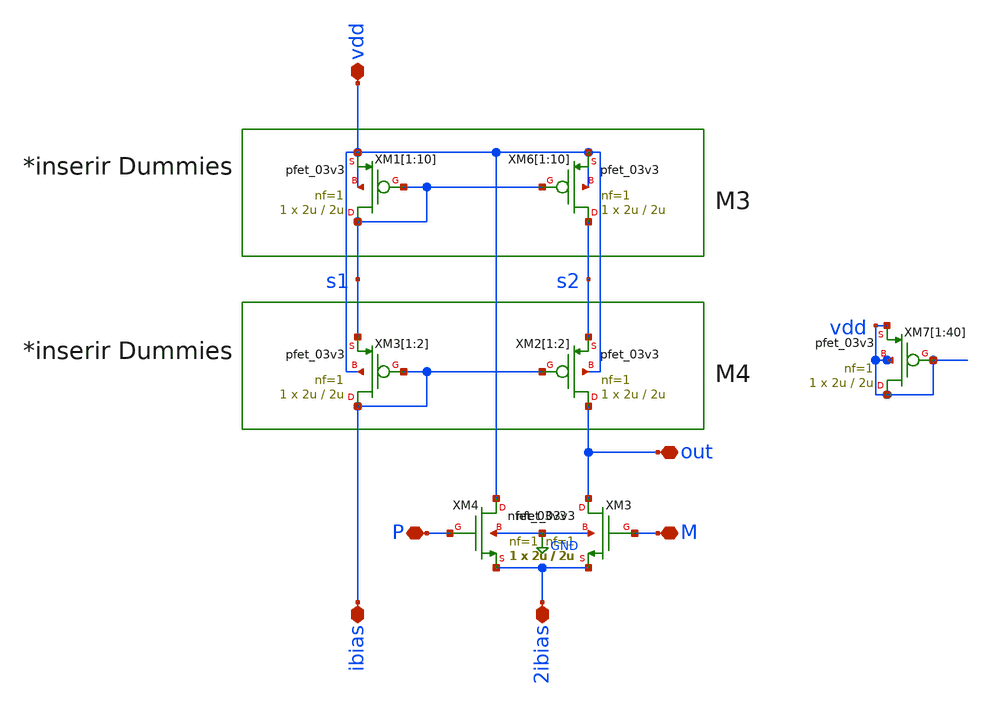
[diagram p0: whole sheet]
** sch_path: Clock_Reference/symbols_clock/VCIS.sch
**.subckt VCIS 2ibias ibias P M out vdd
*.iopin 2ibias
*.iopin ibias
*.iopin P
*.iopin M
*.iopin out
*.iopin vdd
XM2[1] out ibias s2 vdd pfet_03v3 L=2u W=2u nf=1 ad='int((nf+1)/2) * W/nf * 0.18u' as='int((nf+2)/2) * W/nf * 0.18u'
+ pd='2*int((nf+1)/2) * (W/nf + 0.18u)' ps='2*int((nf+2)/2) * (W/nf + 0.18u)' nrd='0.18u / W' nrs='0.18u / W'
+ sa=0 sb=0 sd=0 m=1
XM2[2] out ibias s2 vdd pfet_03v3 L=2u W=2u nf=1 ad='int((nf+1)/2) * W/nf * 0.18u' as='int((nf+2)/2) * W/nf * 0.18u'
+ pd='2*int((nf+1)/2) * (W/nf + 0.18u)' ps='2*int((nf+2)/2) * (W/nf + 0.18u)' nrd='0.18u / W' nrs='0.18u / W'
+ sa=0 sb=0 sd=0 m=1
XM3[1] ibias ibias s1 vdd pfet_03v3 L=2u W=2u nf=1 ad='int((nf+1)/2) * W/nf * 0.18u' as='int((nf+2)/2) * W/nf * 0.18u'
+ pd='2*int((nf+1)/2) * (W/nf + 0.18u)' ps='2*int((nf+2)/2) * (W/nf + 0.18u)' nrd='0.18u / W' nrs='0.18u / W'
+ sa=0 sb=0 sd=0 m=1
XM3[2] ibias ibias s1 vdd pfet_03v3 L=2u W=2u nf=1 ad='int((nf+1)/2) * W/nf * 0.18u' as='int((nf+2)/2) * W/nf * 0.18u'
+ pd='2*int((nf+1)/2) * (W/nf + 0.18u)' ps='2*int((nf+2)/2) * (W/nf + 0.18u)' nrd='0.18u / W' nrs='0.18u / W'
+ sa=0 sb=0 sd=0 m=1
XM3 out M 2ibias GND nfet_03v3 L=2u W=2u nf=1 ad='int((nf+1)/2) * W/nf * 0.18u' as='int((nf+2)/2) * W/nf * 0.18u'
+ pd='2*int((nf+1)/2) * (W/nf + 0.18u)' ps='2*int((nf+2)/2) * (W/nf + 0.18u)' nrd='0.18u / W' nrs='0.18u / W'
+ sa=0 sb=0 sd=0 m=1
XM4 vdd P 2ibias GND nfet_03v3 L=2u W=2u nf=1 ad='int((nf+1)/2) * W/nf * 0.18u' as='int((nf+2)/2) * W/nf * 0.18u'
+ pd='2*int((nf+1)/2) * (W/nf + 0.18u)' ps='2*int((nf+2)/2) * (W/nf + 0.18u)' nrd='0.18u / W' nrs='0.18u / W'
+ sa=0 sb=0 sd=0 m=1
XM6[1] s2 s1 vdd vdd pfet_03v3 L=2u W=2u nf=1 ad='int((nf+1)/2) * W/nf * 0.18u' as='int((nf+2)/2) * W/nf * 0.18u'
+ pd='2*int((nf+1)/2) * (W/nf + 0.18u)' ps='2*int((nf+2)/2) * (W/nf + 0.18u)' nrd='0.18u / W' nrs='0.18u / W'
+ sa=0 sb=0 sd=0 m=1
XM6[2] s2 s1 vdd vdd pfet_03v3 L=2u W=2u nf=1 ad='int((nf+1)/2) * W/nf * 0.18u' as='int((nf+2)/2) * W/nf * 0.18u'
+ pd='2*int((nf+1)/2) * (W/nf + 0.18u)' ps='2*int((nf+2)/2) * (W/nf + 0.18u)' nrd='0.18u / W' nrs='0.18u / W'
+ sa=0 sb=0 sd=0 m=1
XM6[3] s2 s1 vdd vdd pfet_03v3 L=2u W=2u nf=1 ad='int((nf+1)/2) * W/nf * 0.18u' as='int((nf+2)/2) * W/nf * 0.18u'
+ pd='2*int((nf+1)/2) * (W/nf + 0.18u)' ps='2*int((nf+2)/2) * (W/nf + 0.18u)' nrd='0.18u / W' nrs='0.18u / W'
+ sa=0 sb=0 sd=0 m=1
XM6[4] s2 s1 vdd vdd pfet_03v3 L=2u W=2u nf=1 ad='int((nf+1)/2) * W/nf * 0.18u' as='int((nf+2)/2) * W/nf * 0.18u'
+ pd='2*int((nf+1)/2) * (W/nf + 0.18u)' ps='2*int((nf+2)/2) * (W/nf + 0.18u)' nrd='0.18u / W' nrs='0.18u / W'
+ sa=0 sb=0 sd=0 m=1
XM6[5] s2 s1 vdd vdd pfet_03v3 L=2u W=2u nf=1 ad='int((nf+1)/2) * W/nf * 0.18u' as='int((nf+2)/2) * W/nf * 0.18u'
+ pd='2*int((nf+1)/2) * (W/nf + 0.18u)' ps='2*int((nf+2)/2) * (W/nf + 0.18u)' nrd='0.18u / W' nrs='0.18u / W'
+ sa=0 sb=0 sd=0 m=1
XM6[6] s2 s1 vdd vdd pfet_03v3 L=2u W=2u nf=1 ad='int((nf+1)/2) * W/nf * 0.18u' as='int((nf+2)/2) * W/nf * 0.18u'
+ pd='2*int((nf+1)/2) * (W/nf + 0.18u)' ps='2*int((nf+2)/2) * (W/nf + 0.18u)' nrd='0.18u / W' nrs='0.18u / W'
+ sa=0 sb=0 sd=0 m=1
XM6[7] s2 s1 vdd vdd pfet_03v3 L=2u W=2u nf=1 ad='int((nf+1)/2) * W/nf * 0.18u' as='int((nf+2)/2) * W/nf * 0.18u'
+ pd='2*int((nf+1)/2) * (W/nf + 0.18u)' ps='2*int((nf+2)/2) * (W/nf + 0.18u)' nrd='0.18u / W' nrs='0.18u / W'
+ sa=0 sb=0 sd=0 m=1
XM6[8] s2 s1 vdd vdd pfet_03v3 L=2u W=2u nf=1 ad='int((nf+1)/2) * W/nf * 0.18u' as='int((nf+2)/2) * W/nf * 0.18u'
+ pd='2*int((nf+1)/2) * (W/nf + 0.18u)' ps='2*int((nf+2)/2) * (W/nf + 0.18u)' nrd='0.18u / W' nrs='0.18u / W'
+ sa=0 sb=0 sd=0 m=1
XM6[9] s2 s1 vdd vdd pfet_03v3 L=2u W=2u nf=1 ad='int((nf+1)/2) * W/nf * 0.18u' as='int((nf+2)/2) * W/nf * 0.18u'
+ pd='2*int((nf+1)/2) * (W/nf + 0.18u)' ps='2*int((nf+2)/2) * (W/nf + 0.18u)' nrd='0.18u / W' nrs='0.18u / W'
+ sa=0 sb=0 sd=0 m=1
XM6[10] s2 s1 vdd vdd pfet_03v3 L=2u W=2u nf=1 ad='int((nf+1)/2) * W/nf * 0.18u' as='int((nf+2)/2) * W/nf * 0.18u'
+ pd='2*int((nf+1)/2) * (W/nf + 0.18u)' ps='2*int((nf+2)/2) * (W/nf + 0.18u)' nrd='0.18u / W' nrs='0.18u / W'
+ sa=0 sb=0 sd=0 m=1
XM1[1] s1 s1 vdd vdd pfet_03v3 L=2u W=2u nf=1 ad='int((nf+1)/2) * W/nf * 0.18u' as='int((nf+2)/2) * W/nf * 0.18u'
+ pd='2*int((nf+1)/2) * (W/nf + 0.18u)' ps='2*int((nf+2)/2) * (W/nf + 0.18u)' nrd='0.18u / W' nrs='0.18u / W'
+ sa=0 sb=0 sd=0 m=1
XM1[2] s1 s1 vdd vdd pfet_03v3 L=2u W=2u nf=1 ad='int((nf+1)/2) * W/nf * 0.18u' as='int((nf+2)/2) * W/nf * 0.18u'
+ pd='2*int((nf+1)/2) * (W/nf + 0.18u)' ps='2*int((nf+2)/2) * (W/nf + 0.18u)' nrd='0.18u / W' nrs='0.18u / W'
+ sa=0 sb=0 sd=0 m=1
XM1[3] s1 s1 vdd vdd pfet_03v3 L=2u W=2u nf=1 ad='int((nf+1)/2) * W/nf * 0.18u' as='int((nf+2)/2) * W/nf * 0.18u'
+ pd='2*int((nf+1)/2) * (W/nf + 0.18u)' ps='2*int((nf+2)/2) * (W/nf + 0.18u)' nrd='0.18u / W' nrs='0.18u / W'
+ sa=0 sb=0 sd=0 m=1
XM1[4] s1 s1 vdd vdd pfet_03v3 L=2u W=2u nf=1 ad='int((nf+1)/2) * W/nf * 0.18u' as='int((nf+2)/2) * W/nf * 0.18u'
+ pd='2*int((nf+1)/2) * (W/nf + 0.18u)' ps='2*int((nf+2)/2) * (W/nf + 0.18u)' nrd='0.18u / W' nrs='0.18u / W'
+ sa=0 sb=0 sd=0 m=1
XM1[5] s1 s1 vdd vdd pfet_03v3 L=2u W=2u nf=1 ad='int((nf+1)/2) * W/nf * 0.18u' as='int((nf+2)/2) * W/nf * 0.18u'
+ pd='2*int((nf+1)/2) * (W/nf + 0.18u)' ps='2*int((nf+2)/2) * (W/nf + 0.18u)' nrd='0.18u / W' nrs='0.18u / W'
+ sa=0 sb=0 sd=0 m=1
XM1[6] s1 s1 vdd vdd pfet_03v3 L=2u W=2u nf=1 ad='int((nf+1)/2) * W/nf * 0.18u' as='int((nf+2)/2) * W/nf * 0.18u'
+ pd='2*int((nf+1)/2) * (W/nf + 0.18u)' ps='2*int((nf+2)/2) * (W/nf + 0.18u)' nrd='0.18u / W' nrs='0.18u / W'
+ sa=0 sb=0 sd=0 m=1
XM1[7] s1 s1 vdd vdd pfet_03v3 L=2u W=2u nf=1 ad='int((nf+1)/2) * W/nf * 0.18u' as='int((nf+2)/2) * W/nf * 0.18u'
+ pd='2*int((nf+1)/2) * (W/nf + 0.18u)' ps='2*int((nf+2)/2) * (W/nf + 0.18u)' nrd='0.18u / W' nrs='0.18u / W'
+ sa=0 sb=0 sd=0 m=1
XM1[8] s1 s1 vdd vdd pfet_03v3 L=2u W=2u nf=1 ad='int((nf+1)/2) * W/nf * 0.18u' as='int((nf+2)/2) * W/nf * 0.18u'
+ pd='2*int((nf+1)/2) * (W/nf + 0.18u)' ps='2*int((nf+2)/2) * (W/nf + 0.18u)' nrd='0.18u / W' nrs='0.18u / W'
+ sa=0 sb=0 sd=0 m=1
XM1[9] s1 s1 vdd vdd pfet_03v3 L=2u W=2u nf=1 ad='int((nf+1)/2) * W/nf * 0.18u' as='int((nf+2)/2) * W/nf * 0.18u'
+ pd='2*int((nf+1)/2) * (W/nf + 0.18u)' ps='2*int((nf+2)/2) * (W/nf + 0.18u)' nrd='0.18u / W' nrs='0.18u / W'
+ sa=0 sb=0 sd=0 m=1
XM1[10] s1 s1 vdd vdd pfet_03v3 L=2u W=2u nf=1 ad='int((nf+1)/2) * W/nf * 0.18u' as='int((nf+2)/2) * W/nf * 0.18u'
+ pd='2*int((nf+1)/2) * (W/nf + 0.18u)' ps='2*int((nf+2)/2) * (W/nf + 0.18u)' nrd='0.18u / W' nrs='0.18u / W'
+ sa=0 sb=0 sd=0 m=1
XM7[1] vdd vdd vdd vdd pfet_03v3 L=2u W=2u nf=1 ad='int((nf+1)/2) * W/nf * 0.18u' as='int((nf+2)/2) * W/nf * 0.18u'
+ pd='2*int((nf+1)/2) * (W/nf + 0.18u)' ps='2*int((nf+2)/2) * (W/nf + 0.18u)' nrd='0.18u / W' nrs='0.18u / W'
+ sa=0 sb=0 sd=0 m=1
XM7[2] vdd vdd vdd vdd pfet_03v3 L=2u W=2u nf=1 ad='int((nf+1)/2) * W/nf * 0.18u' as='int((nf+2)/2) * W/nf * 0.18u'
+ pd='2*int((nf+1)/2) * (W/nf + 0.18u)' ps='2*int((nf+2)/2) * (W/nf + 0.18u)' nrd='0.18u / W' nrs='0.18u / W'
+ sa=0 sb=0 sd=0 m=1
XM7[3] vdd vdd vdd vdd pfet_03v3 L=2u W=2u nf=1 ad='int((nf+1)/2) * W/nf * 0.18u' as='int((nf+2)/2) * W/nf * 0.18u'
+ pd='2*int((nf+1)/2) * (W/nf + 0.18u)' ps='2*int((nf+2)/2) * (W/nf + 0.18u)' nrd='0.18u / W' nrs='0.18u / W'
+ sa=0 sb=0 sd=0 m=1
XM7[4] vdd vdd vdd vdd pfet_03v3 L=2u W=2u nf=1 ad='int((nf+1)/2) * W/nf * 0.18u' as='int((nf+2)/2) * W/nf * 0.18u'
+ pd='2*int((nf+1)/2) * (W/nf + 0.18u)' ps='2*int((nf+2)/2) * (W/nf + 0.18u)' nrd='0.18u / W' nrs='0.18u / W'
+ sa=0 sb=0 sd=0 m=1
XM7[5] vdd vdd vdd vdd pfet_03v3 L=2u W=2u nf=1 ad='int((nf+1)/2) * W/nf * 0.18u' as='int((nf+2)/2) * W/nf * 0.18u'
+ pd='2*int((nf+1)/2) * (W/nf + 0.18u)' ps='2*int((nf+2)/2) * (W/nf + 0.18u)' nrd='0.18u / W' nrs='0.18u / W'
+ sa=0 sb=0 sd=0 m=1
XM7[6] vdd vdd vdd vdd pfet_03v3 L=2u W=2u nf=1 ad='int((nf+1)/2) * W/nf * 0.18u' as='int((nf+2)/2) * W/nf * 0.18u'
+ pd='2*int((nf+1)/2) * (W/nf + 0.18u)' ps='2*int((nf+2)/2) * (W/nf + 0.18u)' nrd='0.18u / W' nrs='0.18u / W'
+ sa=0 sb=0 sd=0 m=1
XM7[7] vdd vdd vdd vdd pfet_03v3 L=2u W=2u nf=1 ad='int((nf+1)/2) * W/nf * 0.18u' as='int((nf+2)/2) * W/nf * 0.18u'
+ pd='2*int((nf+1)/2) * (W/nf + 0.18u)' ps='2*int((nf+2)/2) * (W/nf + 0.18u)' nrd='0.18u / W' nrs='0.18u / W'
+ sa=0 sb=0 sd=0 m=1
XM7[8] vdd vdd vdd vdd pfet_03v3 L=2u W=2u nf=1 ad='int((nf+1)/2) * W/nf * 0.18u' as='int((nf+2)/2) * W/nf * 0.18u'
+ pd='2*int((nf+1)/2) * (W/nf + 0.18u)' ps='2*int((nf+2)/2) * (W/nf + 0.18u)' nrd='0.18u / W' nrs='0.18u / W'
+ sa=0 sb=0 sd=0 m=1
XM7[9] vdd vdd vdd vdd pfet_03v3 L=2u W=2u nf=1 ad='int((nf+1)/2) * W/nf * 0.18u' as='int((nf+2)/2) * W/nf * 0.18u'
+ pd='2*int((nf+1)/2) * (W/nf + 0.18u)' ps='2*int((nf+2)/2) * (W/nf + 0.18u)' nrd='0.18u / W' nrs='0.18u / W'
+ sa=0 sb=0 sd=0 m=1
XM7[10] vdd vdd vdd vdd pfet_03v3 L=2u W=2u nf=1 ad='int((nf+1)/2) * W/nf * 0.18u' as='int((nf+2)/2) * W/nf * 0.18u'
+ pd='2*int((nf+1)/2) * (W/nf + 0.18u)' ps='2*int((nf+2)/2) * (W/nf + 0.18u)' nrd='0.18u / W' nrs='0.18u / W'
+ sa=0 sb=0 sd=0 m=1
XM7[11] vdd vdd vdd vdd pfet_03v3 L=2u W=2u nf=1 ad='int((nf+1)/2) * W/nf * 0.18u' as='int((nf+2)/2) * W/nf * 0.18u'
+ pd='2*int((nf+1)/2) * (W/nf + 0.18u)' ps='2*int((nf+2)/2) * (W/nf + 0.18u)' nrd='0.18u / W' nrs='0.18u / W'
+ sa=0 sb=0 sd=0 m=1
XM7[12] vdd vdd vdd vdd pfet_03v3 L=2u W=2u nf=1 ad='int((nf+1)/2) * W/nf * 0.18u' as='int((nf+2)/2) * W/nf * 0.18u'
+ pd='2*int((nf+1)/2) * (W/nf + 0.18u)' ps='2*int((nf+2)/2) * (W/nf + 0.18u)' nrd='0.18u / W' nrs='0.18u / W'
+ sa=0 sb=0 sd=0 m=1
XM7[13] vdd vdd vdd vdd pfet_03v3 L=2u W=2u nf=1 ad='int((nf+1)/2) * W/nf * 0.18u' as='int((nf+2)/2) * W/nf * 0.18u'
+ pd='2*int((nf+1)/2) * (W/nf + 0.18u)' ps='2*int((nf+2)/2) * (W/nf + 0.18u)' nrd='0.18u / W' nrs='0.18u / W'
+ sa=0 sb=0 sd=0 m=1
XM7[14] vdd vdd vdd vdd pfet_03v3 L=2u W=2u nf=1 ad='int((nf+1)/2) * W/nf * 0.18u' as='int((nf+2)/2) * W/nf * 0.18u'
+ pd='2*int((nf+1)/2) * (W/nf + 0.18u)' ps='2*int((nf+2)/2) * (W/nf + 0.18u)' nrd='0.18u / W' nrs='0.18u / W'
+ sa=0 sb=0 sd=0 m=1
XM7[15] vdd vdd vdd vdd pfet_03v3 L=2u W=2u nf=1 ad='int((nf+1)/2) * W/nf * 0.18u' as='int((nf+2)/2) * W/nf * 0.18u'
+ pd='2*int((nf+1)/2) * (W/nf + 0.18u)' ps='2*int((nf+2)/2) * (W/nf + 0.18u)' nrd='0.18u / W' nrs='0.18u / W'
+ sa=0 sb=0 sd=0 m=1
XM7[16] vdd vdd vdd vdd pfet_03v3 L=2u W=2u nf=1 ad='int((nf+1)/2) * W/nf * 0.18u' as='int((nf+2)/2) * W/nf * 0.18u'
+ pd='2*int((nf+1)/2) * (W/nf + 0.18u)' ps='2*int((nf+2)/2) * (W/nf + 0.18u)' nrd='0.18u / W' nrs='0.18u / W'
+ sa=0 sb=0 sd=0 m=1
XM7[17] vdd vdd vdd vdd pfet_03v3 L=2u W=2u nf=1 ad='int((nf+1)/2) * W/nf * 0.18u' as='int((nf+2)/2) * W/nf * 0.18u'
+ pd='2*int((nf+1)/2) * (W/nf + 0.18u)' ps='2*int((nf+2)/2) * (W/nf + 0.18u)' nrd='0.18u / W' nrs='0.18u / W'
+ sa=0 sb=0 sd=0 m=1
XM7[18] vdd vdd vdd vdd pfet_03v3 L=2u W=2u nf=1 ad='int((nf+1)/2) * W/nf * 0.18u' as='int((nf+2)/2) * W/nf * 0.18u'
+ pd='2*int((nf+1)/2) * (W/nf + 0.18u)' ps='2*int((nf+2)/2) * (W/nf + 0.18u)' nrd='0.18u / W' nrs='0.18u / W'
+ sa=0 sb=0 sd=0 m=1
XM7[19] vdd vdd vdd vdd pfet_03v3 L=2u W=2u nf=1 ad='int((nf+1)/2) * W/nf * 0.18u' as='int((nf+2)/2) * W/nf * 0.18u'
+ pd='2*int((nf+1)/2) * (W/nf + 0.18u)' ps='2*int((nf+2)/2) * (W/nf + 0.18u)' nrd='0.18u / W' nrs='0.18u / W'
+ sa=0 sb=0 sd=0 m=1
XM7[20] vdd vdd vdd vdd pfet_03v3 L=2u W=2u nf=1 ad='int((nf+1)/2) * W/nf * 0.18u' as='int((nf+2)/2) * W/nf * 0.18u'
+ pd='2*int((nf+1)/2) * (W/nf + 0.18u)' ps='2*int((nf+2)/2) * (W/nf + 0.18u)' nrd='0.18u / W' nrs='0.18u / W'
+ sa=0 sb=0 sd=0 m=1
XM7[21] vdd vdd vdd vdd pfet_03v3 L=2u W=2u nf=1 ad='int((nf+1)/2) * W/nf * 0.18u' as='int((nf+2)/2) * W/nf * 0.18u'
+ pd='2*int((nf+1)/2) * (W/nf + 0.18u)' ps='2*int((nf+2)/2) * (W/nf + 0.18u)' nrd='0.18u / W' nrs='0.18u / W'
+ sa=0 sb=0 sd=0 m=1
XM7[22] vdd vdd vdd vdd pfet_03v3 L=2u W=2u nf=1 ad='int((nf+1)/2) * W/nf * 0.18u' as='int((nf+2)/2) * W/nf * 0.18u'
+ pd='2*int((nf+1)/2) * (W/nf + 0.18u)' ps='2*int((nf+2)/2) * (W/nf + 0.18u)' nrd='0.18u / W' nrs='0.18u / W'
+ sa=0 sb=0 sd=0 m=1
XM7[23] vdd vdd vdd vdd pfet_03v3 L=2u W=2u nf=1 ad='int((nf+1)/2) * W/nf * 0.18u' as='int((nf+2)/2) * W/nf * 0.18u'
+ pd='2*int((nf+1)/2) * (W/nf + 0.18u)' ps='2*int((nf+2)/2) * (W/nf + 0.18u)' nrd='0.18u / W' nrs='0.18u / W'
+ sa=0 sb=0 sd=0 m=1
XM7[24] vdd vdd vdd vdd pfet_03v3 L=2u W=2u nf=1 ad='int((nf+1)/2) * W/nf * 0.18u' as='int((nf+2)/2) * W/nf * 0.18u'
+ pd='2*int((nf+1)/2) * (W/nf + 0.18u)' ps='2*int((nf+2)/2) * (W/nf + 0.18u)' nrd='0.18u / W' nrs='0.18u / W'
+ sa=0 sb=0 sd=0 m=1
XM7[25] vdd vdd vdd vdd pfet_03v3 L=2u W=2u nf=1 ad='int((nf+1)/2) * W/nf * 0.18u' as='int((nf+2)/2) * W/nf * 0.18u'
+ pd='2*int((nf+1)/2) * (W/nf + 0.18u)' ps='2*int((nf+2)/2) * (W/nf + 0.18u)' nrd='0.18u / W' nrs='0.18u / W'
+ sa=0 sb=0 sd=0 m=1
XM7[26] vdd vdd vdd vdd pfet_03v3 L=2u W=2u nf=1 ad='int((nf+1)/2) * W/nf * 0.18u' as='int((nf+2)/2) * W/nf * 0.18u'
+ pd='2*int((nf+1)/2) * (W/nf + 0.18u)' ps='2*int((nf+2)/2) * (W/nf + 0.18u)' nrd='0.18u / W' nrs='0.18u / W'
+ sa=0 sb=0 sd=0 m=1
XM7[27] vdd vdd vdd vdd pfet_03v3 L=2u W=2u nf=1 ad='int((nf+1)/2) * W/nf * 0.18u' as='int((nf+2)/2) * W/nf * 0.18u'
+ pd='2*int((nf+1)/2) * (W/nf + 0.18u)' ps='2*int((nf+2)/2) * (W/nf + 0.18u)' nrd='0.18u / W' nrs='0.18u / W'
+ sa=0 sb=0 sd=0 m=1
XM7[28] vdd vdd vdd vdd pfet_03v3 L=2u W=2u nf=1 ad='int((nf+1)/2) * W/nf * 0.18u' as='int((nf+2)/2) * W/nf * 0.18u'
+ pd='2*int((nf+1)/2) * (W/nf + 0.18u)' ps='2*int((nf+2)/2) * (W/nf + 0.18u)' nrd='0.18u / W' nrs='0.18u / W'
+ sa=0 sb=0 sd=0 m=1
XM7[29] vdd vdd vdd vdd pfet_03v3 L=2u W=2u nf=1 ad='int((nf+1)/2) * W/nf * 0.18u' as='int((nf+2)/2) * W/nf * 0.18u'
+ pd='2*int((nf+1)/2) * (W/nf + 0.18u)' ps='2*int((nf+2)/2) * (W/nf + 0.18u)' nrd='0.18u / W' nrs='0.18u / W'
+ sa=0 sb=0 sd=0 m=1
XM7[30] vdd vdd vdd vdd pfet_03v3 L=2u W=2u nf=1 ad='int((nf+1)/2) * W/nf * 0.18u' as='int((nf+2)/2) * W/nf * 0.18u'
+ pd='2*int((nf+1)/2) * (W/nf + 0.18u)' ps='2*int((nf+2)/2) * (W/nf + 0.18u)' nrd='0.18u / W' nrs='0.18u / W'
+ sa=0 sb=0 sd=0 m=1
XM7[31] vdd vdd vdd vdd pfet_03v3 L=2u W=2u nf=1 ad='int((nf+1)/2) * W/nf * 0.18u' as='int((nf+2)/2) * W/nf * 0.18u'
+ pd='2*int((nf+1)/2) * (W/nf + 0.18u)' ps='2*int((nf+2)/2) * (W/nf + 0.18u)' nrd='0.18u / W' nrs='0.18u / W'
+ sa=0 sb=0 sd=0 m=1
XM7[32] vdd vdd vdd vdd pfet_03v3 L=2u W=2u nf=1 ad='int((nf+1)/2) * W/nf * 0.18u' as='int((nf+2)/2) * W/nf * 0.18u'
+ pd='2*int((nf+1)/2) * (W/nf + 0.18u)' ps='2*int((nf+2)/2) * (W/nf + 0.18u)' nrd='0.18u / W' nrs='0.18u / W'
+ sa=0 sb=0 sd=0 m=1
XM7[33] vdd vdd vdd vdd pfet_03v3 L=2u W=2u nf=1 ad='int((nf+1)/2) * W/nf * 0.18u' as='int((nf+2)/2) * W/nf * 0.18u'
+ pd='2*int((nf+1)/2) * (W/nf + 0.18u)' ps='2*int((nf+2)/2) * (W/nf + 0.18u)' nrd='0.18u / W' nrs='0.18u / W'
+ sa=0 sb=0 sd=0 m=1
XM7[34] vdd vdd vdd vdd pfet_03v3 L=2u W=2u nf=1 ad='int((nf+1)/2) * W/nf * 0.18u' as='int((nf+2)/2) * W/nf * 0.18u'
+ pd='2*int((nf+1)/2) * (W/nf + 0.18u)' ps='2*int((nf+2)/2) * (W/nf + 0.18u)' nrd='0.18u / W' nrs='0.18u / W'
+ sa=0 sb=0 sd=0 m=1
XM7[35] vdd vdd vdd vdd pfet_03v3 L=2u W=2u nf=1 ad='int((nf+1)/2) * W/nf * 0.18u' as='int((nf+2)/2) * W/nf * 0.18u'
+ pd='2*int((nf+1)/2) * (W/nf + 0.18u)' ps='2*int((nf+2)/2) * (W/nf + 0.18u)' nrd='0.18u / W' nrs='0.18u / W'
+ sa=0 sb=0 sd=0 m=1
XM7[36] vdd vdd vdd vdd pfet_03v3 L=2u W=2u nf=1 ad='int((nf+1)/2) * W/nf * 0.18u' as='int((nf+2)/2) * W/nf * 0.18u'
+ pd='2*int((nf+1)/2) * (W/nf + 0.18u)' ps='2*int((nf+2)/2) * (W/nf + 0.18u)' nrd='0.18u / W' nrs='0.18u / W'
+ sa=0 sb=0 sd=0 m=1
XM7[37] vdd vdd vdd vdd pfet_03v3 L=2u W=2u nf=1 ad='int((nf+1)/2) * W/nf * 0.18u' as='int((nf+2)/2) * W/nf * 0.18u'
+ pd='2*int((nf+1)/2) * (W/nf + 0.18u)' ps='2*int((nf+2)/2) * (W/nf + 0.18u)' nrd='0.18u / W' nrs='0.18u / W'
+ sa=0 sb=0 sd=0 m=1
XM7[38] vdd vdd vdd vdd pfet_03v3 L=2u W=2u nf=1 ad='int((nf+1)/2) * W/nf * 0.18u' as='int((nf+2)/2) * W/nf * 0.18u'
+ pd='2*int((nf+1)/2) * (W/nf + 0.18u)' ps='2*int((nf+2)/2) * (W/nf + 0.18u)' nrd='0.18u / W' nrs='0.18u / W'
+ sa=0 sb=0 sd=0 m=1
XM7[39] vdd vdd vdd vdd pfet_03v3 L=2u W=2u nf=1 ad='int((nf+1)/2) * W/nf * 0.18u' as='int((nf+2)/2) * W/nf * 0.18u'
+ pd='2*int((nf+1)/2) * (W/nf + 0.18u)' ps='2*int((nf+2)/2) * (W/nf + 0.18u)' nrd='0.18u / W' nrs='0.18u / W'
+ sa=0 sb=0 sd=0 m=1
XM7[40] vdd vdd vdd vdd pfet_03v3 L=2u W=2u nf=1 ad='int((nf+1)/2) * W/nf * 0.18u' as='int((nf+2)/2) * W/nf * 0.18u'
+ pd='2*int((nf+1)/2) * (W/nf + 0.18u)' ps='2*int((nf+2)/2) * (W/nf + 0.18u)' nrd='0.18u / W' nrs='0.18u / W'
+ sa=0 sb=0 sd=0 m=1
**.ends
.GLOBAL GND
.end
